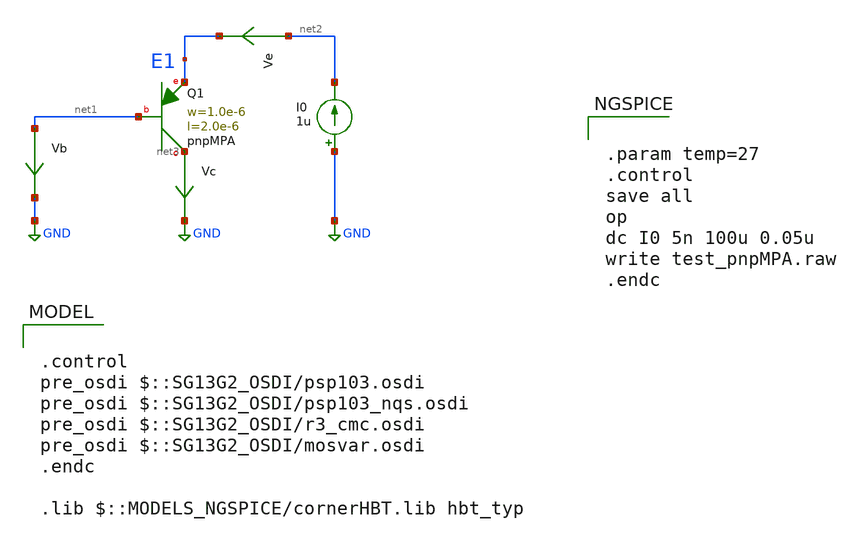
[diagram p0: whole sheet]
** sch_path: ihp-sg13g2/xschem_libs/sg13g2_tests/dc_pnpMPA/schematic/dc_pnpMPA.sch
* Copyright 2023 IHP PDK Authors
**.subckt dc_pnpMPA
Ve net2 E1 0
.save i(ve)
Vb net1 GND 0
.save i(vb)
Vc net3 GND 0
.save i(vc)
I0 GND net2 1u
XQ1 net3 net1 E1 pnpMPA a=2p p=6u m=1
**** begin user architecture code

.control
pre_osdi $::SG13G2_OSDI/psp103.osdi
pre_osdi $::SG13G2_OSDI/psp103_nqs.osdi
pre_osdi $::SG13G2_OSDI/r3_cmc.osdi
pre_osdi $::SG13G2_OSDI/mosvar.osdi
.endc

.lib $::MODELS_NGSPICE/cornerHBT.lib hbt_typ



.param temp=27
.control
save all
op
dc I0 5n 100u 0.05u
write test_pnpMPA.raw
.endc


**** end user architecture code
**.ends
.GLOBAL GND
.end
